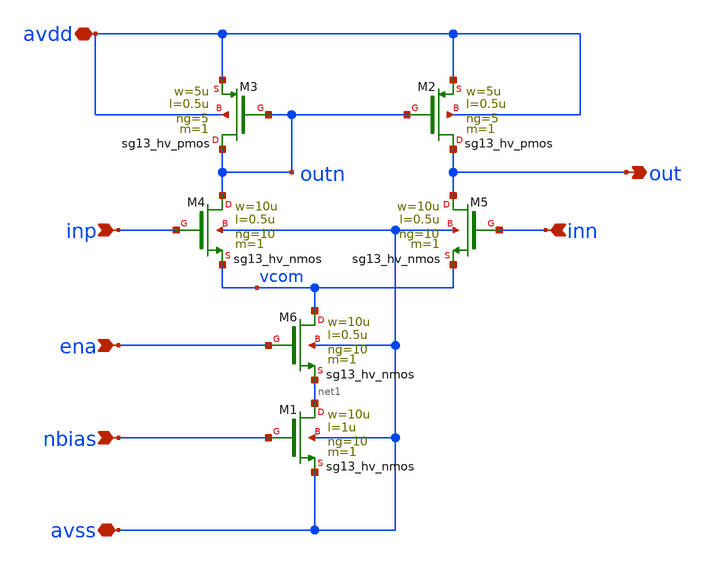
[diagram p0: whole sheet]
** sch_path: xschem/bias_amp.sch
**.subckt bias_amp inp nbias inn out avdd avss ena
*.ipin inp
*.ipin nbias
*.ipin inn
*.opin out
*.iopin avdd
*.iopin avss
*.ipin ena
XM1 net1 nbias avss avss sg13_hv_nmos w=10u l=1u ng=10 m=1 mm_ok=1
XM2 out outn avdd avdd sg13_hv_pmos w=5u l=0.5u ng=5 m=1 mm_ok=1
XM3 outn outn avdd avdd sg13_hv_pmos w=5u l=0.5u ng=5 m=1 mm_ok=1
XM4 outn inp vcom avss sg13_hv_nmos w=10u l=0.5u ng=10 m=1 mm_ok=1
XM5 out inn vcom avss sg13_hv_nmos w=10u l=0.5u ng=10 m=1 mm_ok=1
XM6 vcom ena net1 avss sg13_hv_nmos w=10u l=0.5u ng=10 m=1 mm_ok=1
**.ends
.end
